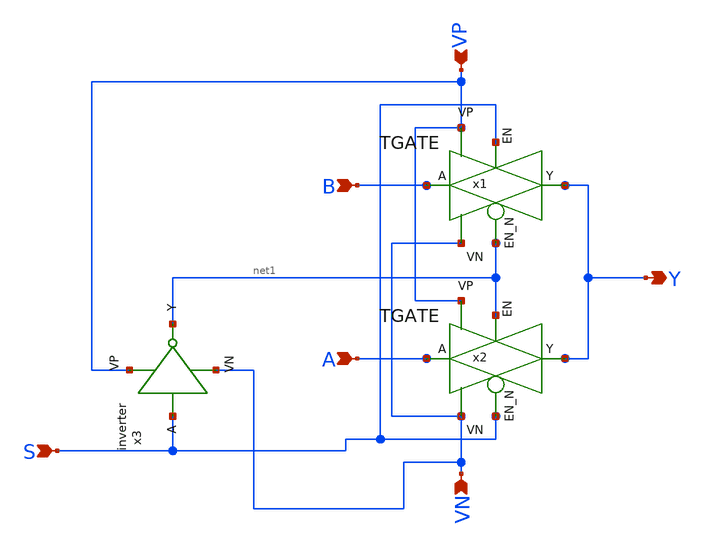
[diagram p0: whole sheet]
** sch_path: ADC/4bit_C2C/MagicAndSpice/EE431_FinalProj/MUX_2_1.sch
**.subckt MUX_2_1 A B S Y VN VP
*.ipin A
*.ipin B
*.ipin S
*.opin Y
*.ipin VN
*.ipin VP
x1 B Y S net1 VP VN TGATE
x2 A Y net1 S VP VN TGATE
x3 S net1 VP VN inverter
**.ends
.end
